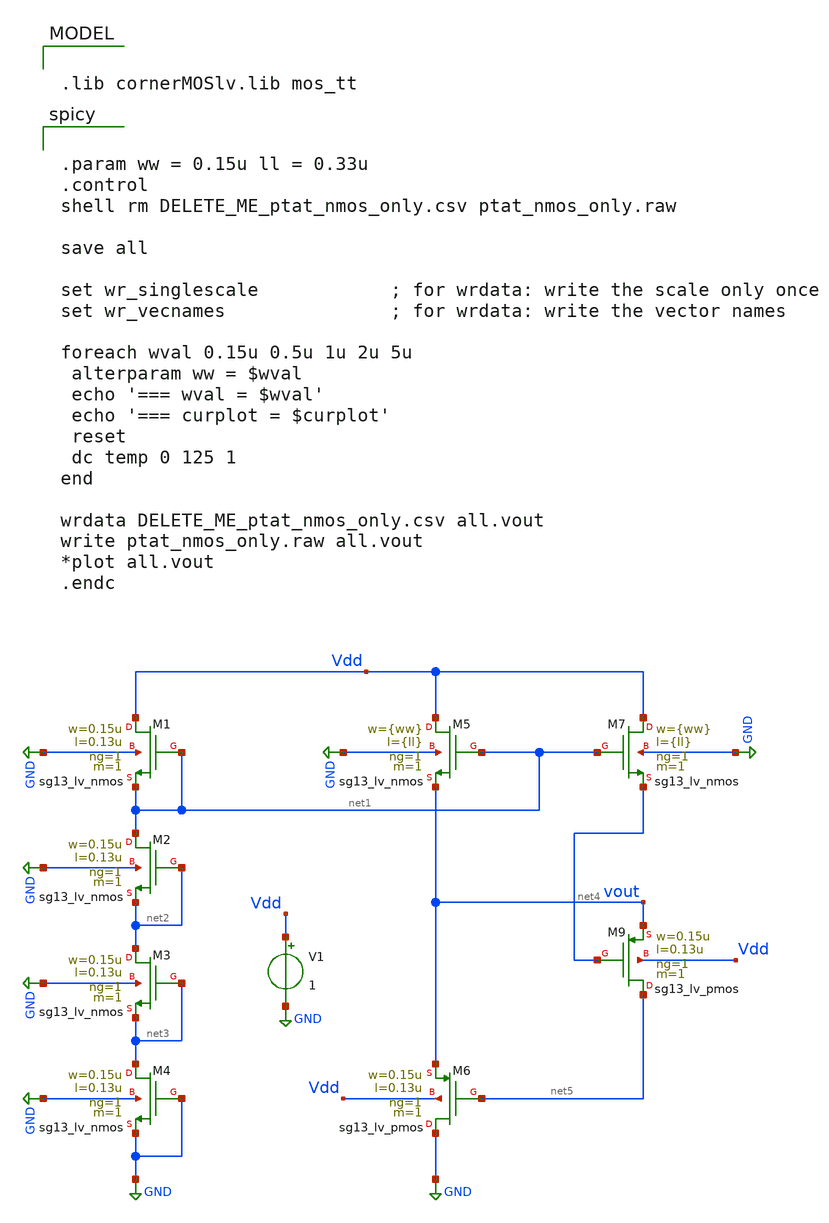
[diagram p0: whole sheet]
** sch_path: TempSensor/design_data/xschem/ptat_nmos_only.sch
**.subckt ptat_nmos_only
XM1 Vdd net1 net1 GND sg13_lv_nmos w=0.15u l=0.13u ng=1 m=1 mm_ok=1
XM2 net1 net2 net2 GND sg13_lv_nmos w=0.15u l=0.13u ng=1 m=1 mm_ok=1
XM3 net2 net3 net3 GND sg13_lv_nmos w=0.15u l=0.13u ng=1 m=1 mm_ok=1
XM4 net3 GND GND GND sg13_lv_nmos w=0.15u l=0.13u ng=1 m=1 mm_ok=1
XM5 Vdd net1 vout GND sg13_lv_nmos w={ww} l={ll} ng=1 m=1 mm_ok=1
XM7 Vdd net1 net4 GND sg13_lv_nmos w={ww} l={ll} ng=1 m=1 mm_ok=1
V1 Vdd GND 1
XM9 net5 net4 vout Vdd sg13_lv_pmos w=0.15u l=0.13u ng=1 m=1 mm_ok=1
XM6 GND net5 vout Vdd sg13_lv_pmos w=0.15u l=0.13u ng=1 m=1 mm_ok=1
**** begin user architecture code

.lib cornerMOSlv.lib mos_tt



.param ww = 0.15u ll = 0.33u
.control
shell rm DELETE_ME_ptat_nmos_only.csv ptat_nmos_only.raw

save all

set wr_singlescale            ; for wrdata: write the scale only once
set wr_vecnames               ; for wrdata: write the vector names

foreach wval 0.15u 0.5u 1u 2u 5u
 alterparam ww = $wval
 echo '=== wval = $wval'
 echo '=== curplot = $curplot'
 reset
 dc temp 0 125 1
end

wrdata DELETE_ME_ptat_nmos_only.csv all.vout
write ptat_nmos_only.raw all.vout
*plot all.vout
.endc


**** end user architecture code
**.ends
.GLOBAL GND
.end
